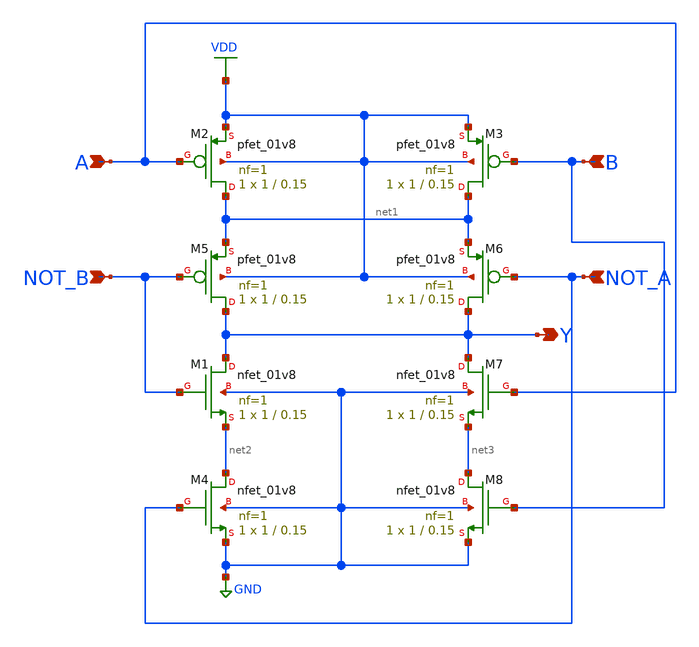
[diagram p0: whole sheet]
** sch_path: library/xschem/xor2.sch
**.subckt xor2 Y A B NOT_A NOT_B
*.opin Y
*.ipin A
*.ipin B
*.ipin NOT_A
*.ipin NOT_B
XM1 Y NOT_B net2 GND sky130_fd_pr__nfet_01v8 L=0.15 W=1 nf=1 ad='int((nf+1)/2) * W/nf * 0.29' as='int((nf+2)/2) * W/nf * 0.29'
+ pd='2*int((nf+1)/2) * (W/nf + 0.29)' ps='2*int((nf+2)/2) * (W/nf + 0.29)' nrd='0.29 / W' nrs='0.29 / W'
+ sa=0 sb=0 sd=0 mult=1 m=1
XM2 net1 A VDD VDD sky130_fd_pr__pfet_01v8 L=0.15 W=1 nf=1 ad='int((nf+1)/2) * W/nf * 0.29' as='int((nf+2)/2) * W/nf * 0.29'
+ pd='2*int((nf+1)/2) * (W/nf + 0.29)' ps='2*int((nf+2)/2) * (W/nf + 0.29)' nrd='0.29 / W' nrs='0.29 / W'
+ sa=0 sb=0 sd=0 mult=1 m=1
XM4 net2 NOT_A GND GND sky130_fd_pr__nfet_01v8 L=0.15 W=1 nf=1 ad='int((nf+1)/2) * W/nf * 0.29' as='int((nf+2)/2) * W/nf * 0.29'
+ pd='2*int((nf+1)/2) * (W/nf + 0.29)' ps='2*int((nf+2)/2) * (W/nf + 0.29)' nrd='0.29 / W' nrs='0.29 / W'
+ sa=0 sb=0 sd=0 mult=1 m=1
XM3 net1 B VDD VDD sky130_fd_pr__pfet_01v8 L=0.15 W=1 nf=1 ad='int((nf+1)/2) * W/nf * 0.29' as='int((nf+2)/2) * W/nf * 0.29'
+ pd='2*int((nf+1)/2) * (W/nf + 0.29)' ps='2*int((nf+2)/2) * (W/nf + 0.29)' nrd='0.29 / W' nrs='0.29 / W'
+ sa=0 sb=0 sd=0 mult=1 m=1
XM5 Y NOT_B net1 VDD sky130_fd_pr__pfet_01v8 L=0.15 W=1 nf=1 ad='int((nf+1)/2) * W/nf * 0.29' as='int((nf+2)/2) * W/nf * 0.29'
+ pd='2*int((nf+1)/2) * (W/nf + 0.29)' ps='2*int((nf+2)/2) * (W/nf + 0.29)' nrd='0.29 / W' nrs='0.29 / W'
+ sa=0 sb=0 sd=0 mult=1 m=1
XM6 Y NOT_A net1 VDD sky130_fd_pr__pfet_01v8 L=0.15 W=1 nf=1 ad='int((nf+1)/2) * W/nf * 0.29' as='int((nf+2)/2) * W/nf * 0.29'
+ pd='2*int((nf+1)/2) * (W/nf + 0.29)' ps='2*int((nf+2)/2) * (W/nf + 0.29)' nrd='0.29 / W' nrs='0.29 / W'
+ sa=0 sb=0 sd=0 mult=1 m=1
XM7 Y A net3 GND sky130_fd_pr__nfet_01v8 L=0.15 W=1 nf=1 ad='int((nf+1)/2) * W/nf * 0.29' as='int((nf+2)/2) * W/nf * 0.29'
+ pd='2*int((nf+1)/2) * (W/nf + 0.29)' ps='2*int((nf+2)/2) * (W/nf + 0.29)' nrd='0.29 / W' nrs='0.29 / W'
+ sa=0 sb=0 sd=0 mult=1 m=1
XM8 net3 B GND GND sky130_fd_pr__nfet_01v8 L=0.15 W=1 nf=1 ad='int((nf+1)/2) * W/nf * 0.29' as='int((nf+2)/2) * W/nf * 0.29'
+ pd='2*int((nf+1)/2) * (W/nf + 0.29)' ps='2*int((nf+2)/2) * (W/nf + 0.29)' nrd='0.29 / W' nrs='0.29 / W'
+ sa=0 sb=0 sd=0 mult=1 m=1
**.ends
.GLOBAL VDD
.GLOBAL GND
.end
